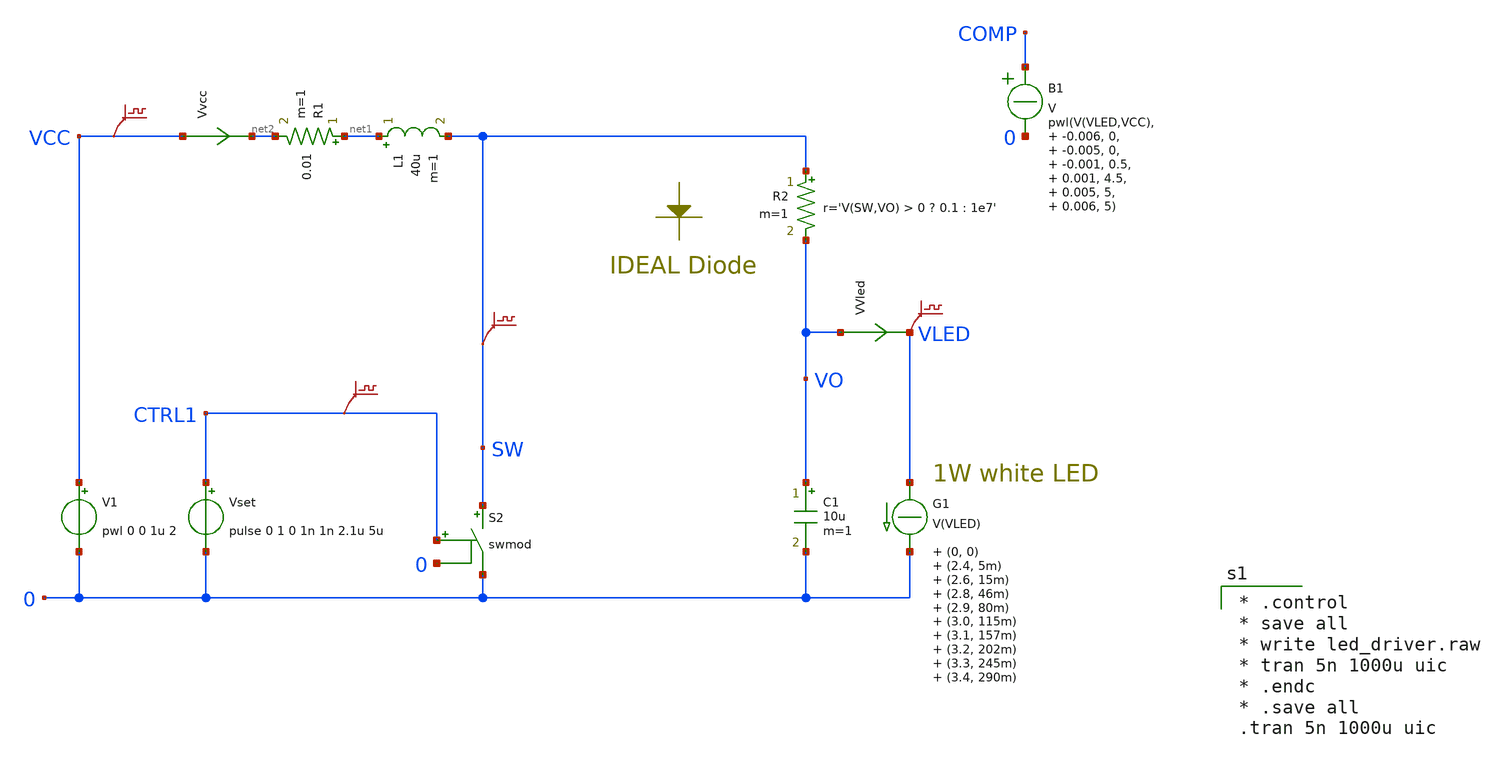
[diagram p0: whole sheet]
** sch_path: xschem_libs_newsym/ngspice/led_driver/schematic/led_driver.sch
* Copyright (C) 1998-2024 Stefan Frederik Schippers
* This program is free software; you can redistribute it and/or modify
* it under the terms of the GNU General Public License as published by
* the Free Software Foundation; either version 2 of the License, or
* (at your option) any later version.
* This program is distributed in the hope that it will be useful,
* but WITHOUT ANY WARRANTY; without even the implied warranty of
* MERCHANTABILITY or FITNESS FOR A PARTICULAR PURPOSE.  See the
* GNU General Public License for more details.
* You should have received a copy of the GNU General Public License
* along with this program; if not, write to the Free Software
**.subckt led_driver
G1 VLED 0 TABLE { V(VLED) } = (0, 0) (2.4, 5m) (2.6, 15m) (2.8, 46m) (2.9, 80m) (3.0, 115m) (3.1, 157m)
+ (3.2, 202m) (3.3, 245m) (3.4, 290m) (3.5, 337m) (3.6, 395m) (3.7, 470m) (4.0, 750m)
V1 VCC 0 pwl 0 0 1u 2
VVled VO VLED 0
.save i(vvled)
S2 SW 0 CTRL1 0 swmod
L1 net1 SW 40u m=1
Vset CTRL1 0 pulse 0 1 0 1n 1n 2.1u 5u
R1 net1 net2 0.01 m=1
C1 VO 0 10u m=1
Vvcc VCC net2 0
.save i(vvcc)
R2 SW VO r='V(SW,VO) > 0 ? 0.1 : 1e7' m=1
B1 COMP 0 V = pwl(V(VLED,VCC), -0.006, 0, -0.005, 0, -0.001, 0.5, 0.001, 4.5, 0.005, 5, 0.006, 5)
.save v(vled)
.save v(vcc)
.save v(sw)
.save v(ctrl1)
**** begin user architecture code

* .control
* save all
* write led_driver.raw
* tran 5n 1000u uic
* .endc
* .save all
.tran 5n 1000u uic



.MODEL DIODE D(IS=1.139e-08 RS=0.99 CJO=9.3e-12 VJ=1.6 M=0.411 BV=30 EG=0.7 )
.MODEL swmod SW(VT=0.1 VH=0.01 RON=0.01 ROFF=10000000)


**** end user architecture code
**.ends
.end
